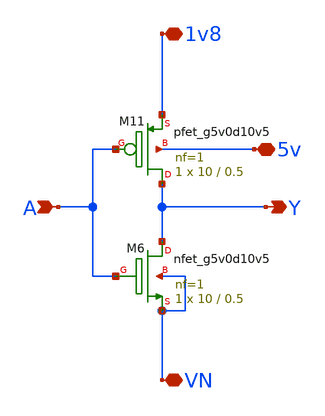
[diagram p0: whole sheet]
** sch_path: ADC/16bit_C2C/MagicAndSpice/inverter_5v_to_1v8.sch
**.subckt inverter_5v_to_1v8 A Y 1v8 VN 5v
*.ipin A
*.opin Y
*.iopin 1v8
*.iopin VN
*.iopin 5v
XM6 Y A VN VN sky130_fd_pr__nfet_g5v0d10v5 L=0.5 W=10 nf=1 ad='int((nf+1)/2) * W/nf * 0.29' as='int((nf+2)/2) * W/nf * 0.29'
+ pd='2*int((nf+1)/2) * (W/nf + 0.29)' ps='2*int((nf+2)/2) * (W/nf + 0.29)' nrd='0.29 / W' nrs='0.29 / W'
+ sa=0 sb=0 sd=0 mult=1 m=1
XM11 Y A 1v8 5v sky130_fd_pr__pfet_g5v0d10v5 L=0.5 W=10 nf=1 ad='int((nf+1)/2) * W/nf * 0.29' as='int((nf+2)/2) * W/nf * 0.29'
+ pd='2*int((nf+1)/2) * (W/nf + 0.29)' ps='2*int((nf+2)/2) * (W/nf + 0.29)' nrd='0.29 / W' nrs='0.29 / W'
+ sa=0 sb=0 sd=0 mult=1 m=1
**.ends
.end
